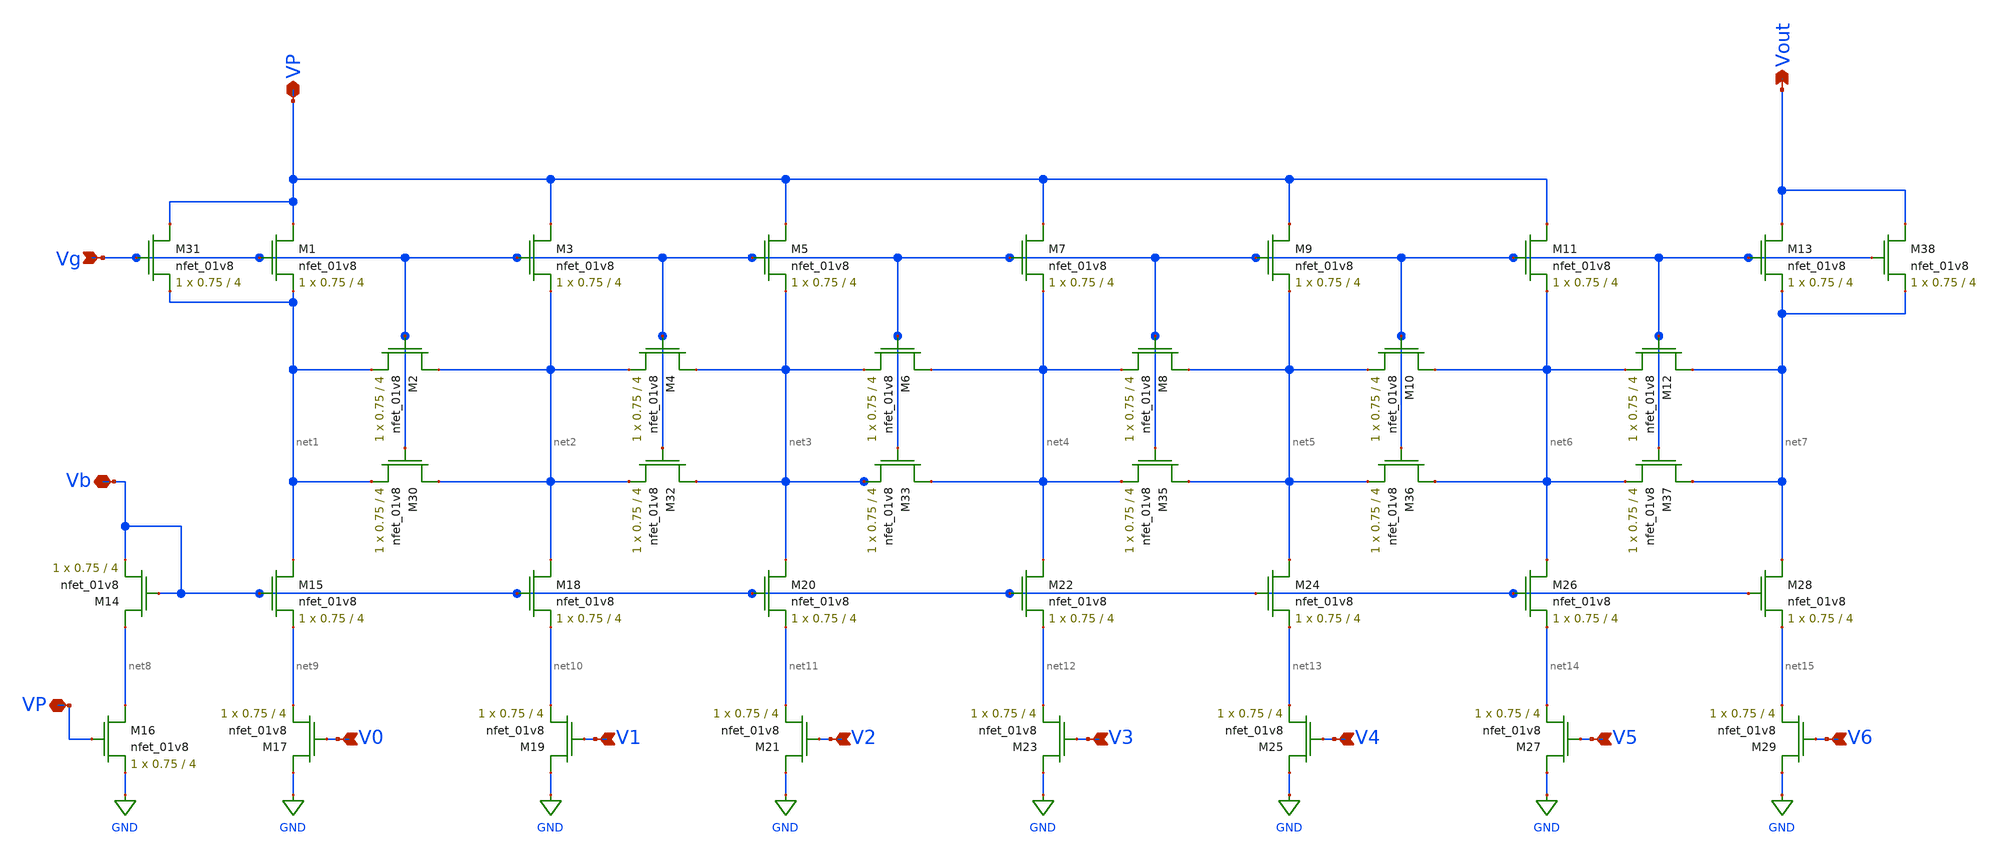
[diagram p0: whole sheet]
** sch_path: MP_4_test_sch.sch
**.subckt MP_4_test_sch Vg VP Vb V6 V5 V4 V3 V2 V1 V0 VP Vout
*.ipin Vg
*.iopin VP
*.iopin Vb
*.ipin V6
*.ipin V5
*.ipin V4
*.ipin V3
*.ipin V2
*.ipin V1
*.ipin V0
*.iopin VP
*.opin Vout
XM1 VP Vg net1 GND sky130_fd_pr__nfet_01v8 L=4 W=0.75 nf=1 ad='int((nf+1)/2) * W/nf * 0.29' as='int((nf+2)/2) * W/nf * 0.29'
+ pd='2*int((nf+1)/2) * (W/nf + 0.29)' ps='2*int((nf+2)/2) * (W/nf + 0.29)' nrd='0.29 / W' nrs='0.29 / W'
+ sa=0 sb=0 sd=0 mult=1 m=1
XM2 net2 Vg net1 GND sky130_fd_pr__nfet_01v8 L=4 W=0.75 nf=1 ad='int((nf+1)/2) * W/nf * 0.29' as='int((nf+2)/2) * W/nf * 0.29'
+ pd='2*int((nf+1)/2) * (W/nf + 0.29)' ps='2*int((nf+2)/2) * (W/nf + 0.29)' nrd='0.29 / W' nrs='0.29 / W'
+ sa=0 sb=0 sd=0 mult=1 m=1
XM3 VP Vg net2 GND sky130_fd_pr__nfet_01v8 L=4 W=0.75 nf=1 ad='int((nf+1)/2) * W/nf * 0.29' as='int((nf+2)/2) * W/nf * 0.29'
+ pd='2*int((nf+1)/2) * (W/nf + 0.29)' ps='2*int((nf+2)/2) * (W/nf + 0.29)' nrd='0.29 / W' nrs='0.29 / W'
+ sa=0 sb=0 sd=0 mult=1 m=1
XM4 net3 Vg net2 GND sky130_fd_pr__nfet_01v8 L=4 W=0.75 nf=1 ad='int((nf+1)/2) * W/nf * 0.29' as='int((nf+2)/2) * W/nf * 0.29'
+ pd='2*int((nf+1)/2) * (W/nf + 0.29)' ps='2*int((nf+2)/2) * (W/nf + 0.29)' nrd='0.29 / W' nrs='0.29 / W'
+ sa=0 sb=0 sd=0 mult=1 m=1
XM5 VP Vg net3 GND sky130_fd_pr__nfet_01v8 L=4 W=0.75 nf=1 ad='int((nf+1)/2) * W/nf * 0.29' as='int((nf+2)/2) * W/nf * 0.29'
+ pd='2*int((nf+1)/2) * (W/nf + 0.29)' ps='2*int((nf+2)/2) * (W/nf + 0.29)' nrd='0.29 / W' nrs='0.29 / W'
+ sa=0 sb=0 sd=0 mult=1 m=1
XM6 net4 Vg net3 GND sky130_fd_pr__nfet_01v8 L=4 W=0.75 nf=1 ad='int((nf+1)/2) * W/nf * 0.29' as='int((nf+2)/2) * W/nf * 0.29'
+ pd='2*int((nf+1)/2) * (W/nf + 0.29)' ps='2*int((nf+2)/2) * (W/nf + 0.29)' nrd='0.29 / W' nrs='0.29 / W'
+ sa=0 sb=0 sd=0 mult=1 m=1
XM7 VP Vg net4 GND sky130_fd_pr__nfet_01v8 L=4 W=0.75 nf=1 ad='int((nf+1)/2) * W/nf * 0.29' as='int((nf+2)/2) * W/nf * 0.29'
+ pd='2*int((nf+1)/2) * (W/nf + 0.29)' ps='2*int((nf+2)/2) * (W/nf + 0.29)' nrd='0.29 / W' nrs='0.29 / W'
+ sa=0 sb=0 sd=0 mult=1 m=1
XM8 net5 Vg net4 GND sky130_fd_pr__nfet_01v8 L=4 W=0.75 nf=1 ad='int((nf+1)/2) * W/nf * 0.29' as='int((nf+2)/2) * W/nf * 0.29'
+ pd='2*int((nf+1)/2) * (W/nf + 0.29)' ps='2*int((nf+2)/2) * (W/nf + 0.29)' nrd='0.29 / W' nrs='0.29 / W'
+ sa=0 sb=0 sd=0 mult=1 m=1
XM9 VP Vg net5 GND sky130_fd_pr__nfet_01v8 L=4 W=0.75 nf=1 ad='int((nf+1)/2) * W/nf * 0.29' as='int((nf+2)/2) * W/nf * 0.29'
+ pd='2*int((nf+1)/2) * (W/nf + 0.29)' ps='2*int((nf+2)/2) * (W/nf + 0.29)' nrd='0.29 / W' nrs='0.29 / W'
+ sa=0 sb=0 sd=0 mult=1 m=1
XM10 net6 Vg net5 GND sky130_fd_pr__nfet_01v8 L=4 W=0.75 nf=1 ad='int((nf+1)/2) * W/nf * 0.29' as='int((nf+2)/2) * W/nf * 0.29'
+ pd='2*int((nf+1)/2) * (W/nf + 0.29)' ps='2*int((nf+2)/2) * (W/nf + 0.29)' nrd='0.29 / W' nrs='0.29 / W'
+ sa=0 sb=0 sd=0 mult=1 m=1
XM11 VP Vg net6 GND sky130_fd_pr__nfet_01v8 L=4 W=0.75 nf=1 ad='int((nf+1)/2) * W/nf * 0.29' as='int((nf+2)/2) * W/nf * 0.29'
+ pd='2*int((nf+1)/2) * (W/nf + 0.29)' ps='2*int((nf+2)/2) * (W/nf + 0.29)' nrd='0.29 / W' nrs='0.29 / W'
+ sa=0 sb=0 sd=0 mult=1 m=1
XM12 net7 Vg net6 GND sky130_fd_pr__nfet_01v8 L=4 W=0.75 nf=1 ad='int((nf+1)/2) * W/nf * 0.29' as='int((nf+2)/2) * W/nf * 0.29'
+ pd='2*int((nf+1)/2) * (W/nf + 0.29)' ps='2*int((nf+2)/2) * (W/nf + 0.29)' nrd='0.29 / W' nrs='0.29 / W'
+ sa=0 sb=0 sd=0 mult=1 m=1
XM13 Vout Vg net7 GND sky130_fd_pr__nfet_01v8 L=4 W=0.75 nf=1 ad='int((nf+1)/2) * W/nf * 0.29' as='int((nf+2)/2) * W/nf * 0.29'
+ pd='2*int((nf+1)/2) * (W/nf + 0.29)' ps='2*int((nf+2)/2) * (W/nf + 0.29)' nrd='0.29 / W' nrs='0.29 / W'
+ sa=0 sb=0 sd=0 mult=1 m=1
XM14 net8 Vb Vb GND sky130_fd_pr__nfet_01v8 L=4 W=0.75 nf=1 ad='int((nf+1)/2) * W/nf * 0.29' as='int((nf+2)/2) * W/nf * 0.29'
+ pd='2*int((nf+1)/2) * (W/nf + 0.29)' ps='2*int((nf+2)/2) * (W/nf + 0.29)' nrd='0.29 / W' nrs='0.29 / W'
+ sa=0 sb=0 sd=0 mult=1 m=1
XM15 net1 Vb net9 GND sky130_fd_pr__nfet_01v8 L=4 W=0.75 nf=1 ad='int((nf+1)/2) * W/nf * 0.29' as='int((nf+2)/2) * W/nf * 0.29'
+ pd='2*int((nf+1)/2) * (W/nf + 0.29)' ps='2*int((nf+2)/2) * (W/nf + 0.29)' nrd='0.29 / W' nrs='0.29 / W'
+ sa=0 sb=0 sd=0 mult=1 m=1
XM16 net8 VP GND GND sky130_fd_pr__nfet_01v8 L=4 W=0.75 nf=1 ad='int((nf+1)/2) * W/nf * 0.29' as='int((nf+2)/2) * W/nf * 0.29'
+ pd='2*int((nf+1)/2) * (W/nf + 0.29)' ps='2*int((nf+2)/2) * (W/nf + 0.29)' nrd='0.29 / W' nrs='0.29 / W'
+ sa=0 sb=0 sd=0 mult=1 m=1
XM17 GND V0 net9 GND sky130_fd_pr__nfet_01v8 L=4 W=0.75 nf=1 ad='int((nf+1)/2) * W/nf * 0.29' as='int((nf+2)/2) * W/nf * 0.29'
+ pd='2*int((nf+1)/2) * (W/nf + 0.29)' ps='2*int((nf+2)/2) * (W/nf + 0.29)' nrd='0.29 / W' nrs='0.29 / W'
+ sa=0 sb=0 sd=0 mult=1 m=1
XM18 net2 Vb net10 GND sky130_fd_pr__nfet_01v8 L=4 W=0.75 nf=1 ad='int((nf+1)/2) * W/nf * 0.29' as='int((nf+2)/2) * W/nf * 0.29'
+ pd='2*int((nf+1)/2) * (W/nf + 0.29)' ps='2*int((nf+2)/2) * (W/nf + 0.29)' nrd='0.29 / W' nrs='0.29 / W'
+ sa=0 sb=0 sd=0 mult=1 m=1
XM19 GND V1 net10 GND sky130_fd_pr__nfet_01v8 L=4 W=0.75 nf=1 ad='int((nf+1)/2) * W/nf * 0.29' as='int((nf+2)/2) * W/nf * 0.29'
+ pd='2*int((nf+1)/2) * (W/nf + 0.29)' ps='2*int((nf+2)/2) * (W/nf + 0.29)' nrd='0.29 / W' nrs='0.29 / W'
+ sa=0 sb=0 sd=0 mult=1 m=1
XM20 net3 Vb net11 GND sky130_fd_pr__nfet_01v8 L=4 W=0.75 nf=1 ad='int((nf+1)/2) * W/nf * 0.29' as='int((nf+2)/2) * W/nf * 0.29'
+ pd='2*int((nf+1)/2) * (W/nf + 0.29)' ps='2*int((nf+2)/2) * (W/nf + 0.29)' nrd='0.29 / W' nrs='0.29 / W'
+ sa=0 sb=0 sd=0 mult=1 m=1
XM21 GND V2 net11 GND sky130_fd_pr__nfet_01v8 L=4 W=0.75 nf=1 ad='int((nf+1)/2) * W/nf * 0.29' as='int((nf+2)/2) * W/nf * 0.29'
+ pd='2*int((nf+1)/2) * (W/nf + 0.29)' ps='2*int((nf+2)/2) * (W/nf + 0.29)' nrd='0.29 / W' nrs='0.29 / W'
+ sa=0 sb=0 sd=0 mult=1 m=1
XM22 net4 Vb net12 GND sky130_fd_pr__nfet_01v8 L=4 W=0.75 nf=1 ad='int((nf+1)/2) * W/nf * 0.29' as='int((nf+2)/2) * W/nf * 0.29'
+ pd='2*int((nf+1)/2) * (W/nf + 0.29)' ps='2*int((nf+2)/2) * (W/nf + 0.29)' nrd='0.29 / W' nrs='0.29 / W'
+ sa=0 sb=0 sd=0 mult=1 m=1
XM23 GND V3 net12 GND sky130_fd_pr__nfet_01v8 L=4 W=0.75 nf=1 ad='int((nf+1)/2) * W/nf * 0.29' as='int((nf+2)/2) * W/nf * 0.29'
+ pd='2*int((nf+1)/2) * (W/nf + 0.29)' ps='2*int((nf+2)/2) * (W/nf + 0.29)' nrd='0.29 / W' nrs='0.29 / W'
+ sa=0 sb=0 sd=0 mult=1 m=1
XM24 net5 Vb net13 GND sky130_fd_pr__nfet_01v8 L=4 W=0.75 nf=1 ad='int((nf+1)/2) * W/nf * 0.29' as='int((nf+2)/2) * W/nf * 0.29'
+ pd='2*int((nf+1)/2) * (W/nf + 0.29)' ps='2*int((nf+2)/2) * (W/nf + 0.29)' nrd='0.29 / W' nrs='0.29 / W'
+ sa=0 sb=0 sd=0 mult=1 m=1
XM25 GND V4 net13 GND sky130_fd_pr__nfet_01v8 L=4 W=0.75 nf=1 ad='int((nf+1)/2) * W/nf * 0.29' as='int((nf+2)/2) * W/nf * 0.29'
+ pd='2*int((nf+1)/2) * (W/nf + 0.29)' ps='2*int((nf+2)/2) * (W/nf + 0.29)' nrd='0.29 / W' nrs='0.29 / W'
+ sa=0 sb=0 sd=0 mult=1 m=1
XM26 net6 Vb net14 GND sky130_fd_pr__nfet_01v8 L=4 W=0.75 nf=1 ad='int((nf+1)/2) * W/nf * 0.29' as='int((nf+2)/2) * W/nf * 0.29'
+ pd='2*int((nf+1)/2) * (W/nf + 0.29)' ps='2*int((nf+2)/2) * (W/nf + 0.29)' nrd='0.29 / W' nrs='0.29 / W'
+ sa=0 sb=0 sd=0 mult=1 m=1
XM27 GND V5 net14 GND sky130_fd_pr__nfet_01v8 L=4 W=0.75 nf=1 ad='int((nf+1)/2) * W/nf * 0.29' as='int((nf+2)/2) * W/nf * 0.29'
+ pd='2*int((nf+1)/2) * (W/nf + 0.29)' ps='2*int((nf+2)/2) * (W/nf + 0.29)' nrd='0.29 / W' nrs='0.29 / W'
+ sa=0 sb=0 sd=0 mult=1 m=1
XM28 net7 Vb net15 GND sky130_fd_pr__nfet_01v8 L=4 W=0.75 nf=1 ad='int((nf+1)/2) * W/nf * 0.29' as='int((nf+2)/2) * W/nf * 0.29'
+ pd='2*int((nf+1)/2) * (W/nf + 0.29)' ps='2*int((nf+2)/2) * (W/nf + 0.29)' nrd='0.29 / W' nrs='0.29 / W'
+ sa=0 sb=0 sd=0 mult=1 m=1
XM29 GND V6 net15 GND sky130_fd_pr__nfet_01v8 L=4 W=0.75 nf=1 ad='int((nf+1)/2) * W/nf * 0.29' as='int((nf+2)/2) * W/nf * 0.29'
+ pd='2*int((nf+1)/2) * (W/nf + 0.29)' ps='2*int((nf+2)/2) * (W/nf + 0.29)' nrd='0.29 / W' nrs='0.29 / W'
+ sa=0 sb=0 sd=0 mult=1 m=1
XM30 net2 Vg net1 GND sky130_fd_pr__nfet_01v8 L=4 W=0.75 nf=1 ad='int((nf+1)/2) * W/nf * 0.29' as='int((nf+2)/2) * W/nf * 0.29'
+ pd='2*int((nf+1)/2) * (W/nf + 0.29)' ps='2*int((nf+2)/2) * (W/nf + 0.29)' nrd='0.29 / W' nrs='0.29 / W'
+ sa=0 sb=0 sd=0 mult=1 m=1
XM31 VP Vg net1 GND sky130_fd_pr__nfet_01v8 L=4 W=0.75 nf=1 ad='int((nf+1)/2) * W/nf * 0.29' as='int((nf+2)/2) * W/nf * 0.29'
+ pd='2*int((nf+1)/2) * (W/nf + 0.29)' ps='2*int((nf+2)/2) * (W/nf + 0.29)' nrd='0.29 / W' nrs='0.29 / W'
+ sa=0 sb=0 sd=0 mult=1 m=1
XM32 net3 Vg net2 GND sky130_fd_pr__nfet_01v8 L=4 W=0.75 nf=1 ad='int((nf+1)/2) * W/nf * 0.29' as='int((nf+2)/2) * W/nf * 0.29'
+ pd='2*int((nf+1)/2) * (W/nf + 0.29)' ps='2*int((nf+2)/2) * (W/nf + 0.29)' nrd='0.29 / W' nrs='0.29 / W'
+ sa=0 sb=0 sd=0 mult=1 m=1
XM33 net4 Vg net3 GND sky130_fd_pr__nfet_01v8 L=4 W=0.75 nf=1 ad='int((nf+1)/2) * W/nf * 0.29' as='int((nf+2)/2) * W/nf * 0.29'
+ pd='2*int((nf+1)/2) * (W/nf + 0.29)' ps='2*int((nf+2)/2) * (W/nf + 0.29)' nrd='0.29 / W' nrs='0.29 / W'
+ sa=0 sb=0 sd=0 mult=1 m=1
XM35 net5 Vg net4 GND sky130_fd_pr__nfet_01v8 L=4 W=0.75 nf=1 ad='int((nf+1)/2) * W/nf * 0.29' as='int((nf+2)/2) * W/nf * 0.29'
+ pd='2*int((nf+1)/2) * (W/nf + 0.29)' ps='2*int((nf+2)/2) * (W/nf + 0.29)' nrd='0.29 / W' nrs='0.29 / W'
+ sa=0 sb=0 sd=0 mult=1 m=1
XM36 net6 Vg net5 GND sky130_fd_pr__nfet_01v8 L=4 W=0.75 nf=1 ad='int((nf+1)/2) * W/nf * 0.29' as='int((nf+2)/2) * W/nf * 0.29'
+ pd='2*int((nf+1)/2) * (W/nf + 0.29)' ps='2*int((nf+2)/2) * (W/nf + 0.29)' nrd='0.29 / W' nrs='0.29 / W'
+ sa=0 sb=0 sd=0 mult=1 m=1
XM37 net7 Vg net6 GND sky130_fd_pr__nfet_01v8 L=4 W=0.75 nf=1 ad='int((nf+1)/2) * W/nf * 0.29' as='int((nf+2)/2) * W/nf * 0.29'
+ pd='2*int((nf+1)/2) * (W/nf + 0.29)' ps='2*int((nf+2)/2) * (W/nf + 0.29)' nrd='0.29 / W' nrs='0.29 / W'
+ sa=0 sb=0 sd=0 mult=1 m=1
XM38 Vout Vg net7 GND sky130_fd_pr__nfet_01v8 L=4 W=0.75 nf=1 ad='int((nf+1)/2) * W/nf * 0.29' as='int((nf+2)/2) * W/nf * 0.29'
+ pd='2*int((nf+1)/2) * (W/nf + 0.29)' ps='2*int((nf+2)/2) * (W/nf + 0.29)' nrd='0.29 / W' nrs='0.29 / W'
+ sa=0 sb=0 sd=0 mult=1 m=1
**.ends
.GLOBAL GND
.end
